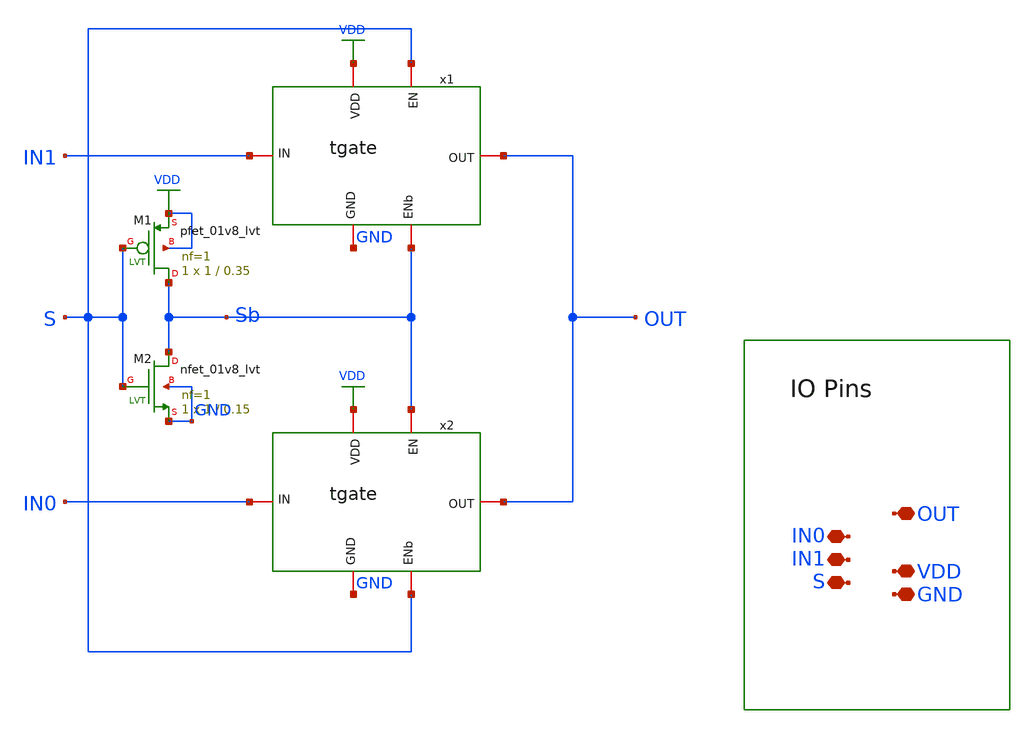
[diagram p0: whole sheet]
** sch_path: scope_sky130_v1/mux2.sch
**.subckt mux2 IN1 VDD GND S OUT IN0
*.iopin IN1
*.iopin VDD
*.iopin GND
*.iopin S
*.iopin OUT
*.iopin IN0
XM1 Sb S VDD VDD sky130_fd_pr__pfet_01v8_lvt L=0.35 W=1 nf=1 ad='int((1 + 1)/2) * 1 / 1 * 0.29' as='int((1 + 2)/2) * 1 / 1 * 0.29'
+ pd='2*int((1 + 1)/2) * (1 / 1 + 0.29)' ps='2*int((1 + 2)/2) * (1 / 1 + 0.29)' nrd='0.29 / 1 ' nrs='0.29 / 1 '
+ sa=0 sb=0 sd=0 mult=1 m=1
XM2 Sb S GND GND sky130_fd_pr__nfet_01v8_lvt L=0.15 W=1 nf=1 ad='int((1 + 1)/2) * 1 / 1 * 0.29' as='int((1 + 2)/2) * 1 / 1 * 0.29'
+ pd='2*int((1 + 1)/2) * (1 / 1 + 0.29)' ps='2*int((1 + 2)/2) * (1 / 1 + 0.29)' nrd='0.29 / 1 ' nrs='0.29 / 1 '
+ sa=0 sb=0 sd=0 mult=1 m=1
x1 IN1 OUT Sb S VDD GND tgate
x2 IN0 OUT S Sb VDD GND tgate
**.ends

* expanding   symbol:  scope_sky130_v1/tgate.sym # of pins=6
** sym_path: scope_sky130_v1/tgate.sym
** sch_path: scope_sky130_v1/tgate.sch
.subckt tgate IN OUT ENb EN VDD GND
*.iopin IN
*.iopin VDD
*.iopin GND
*.iopin ENb
*.iopin EN
*.iopin OUT
XM2 IN EN OUT GND sky130_fd_pr__nfet_01v8 L=0.15 W=0.5 nf=1 ad='int((1 + 1)/2) * 0.5 / 1 * 0.29' as='int((1 + 2)/2) * 0.5 / 1 * 0.29'
+ pd='2*int((1 + 1)/2) * (0.5 / 1 + 0.29)' ps='2*int((1 + 2)/2) * (0.5 / 1 + 0.29)' nrd='0.29 / 0.5 ' nrs='0.29 / 0.5 '
+ sa=0 sb=0 sd=0 mult=1 m=1
XM11 IN ENb OUT VDD sky130_fd_pr__pfet_01v8 L=0.15 W=0.5 nf=1 ad='int((nf+1)/2) * W/nf * 0.29' as='int((nf+2)/2) * W/nf * 0.29'
+ pd='2*int((nf+1)/2) * (W/nf + 0.29)' ps='2*int((nf+2)/2) * (W/nf + 0.29)' nrd='0.29 / W' nrs='0.29 / W'
+ sa=0 sb=0 sd=0 mult=1 m=1
.ends

.GLOBAL VDD
.end
